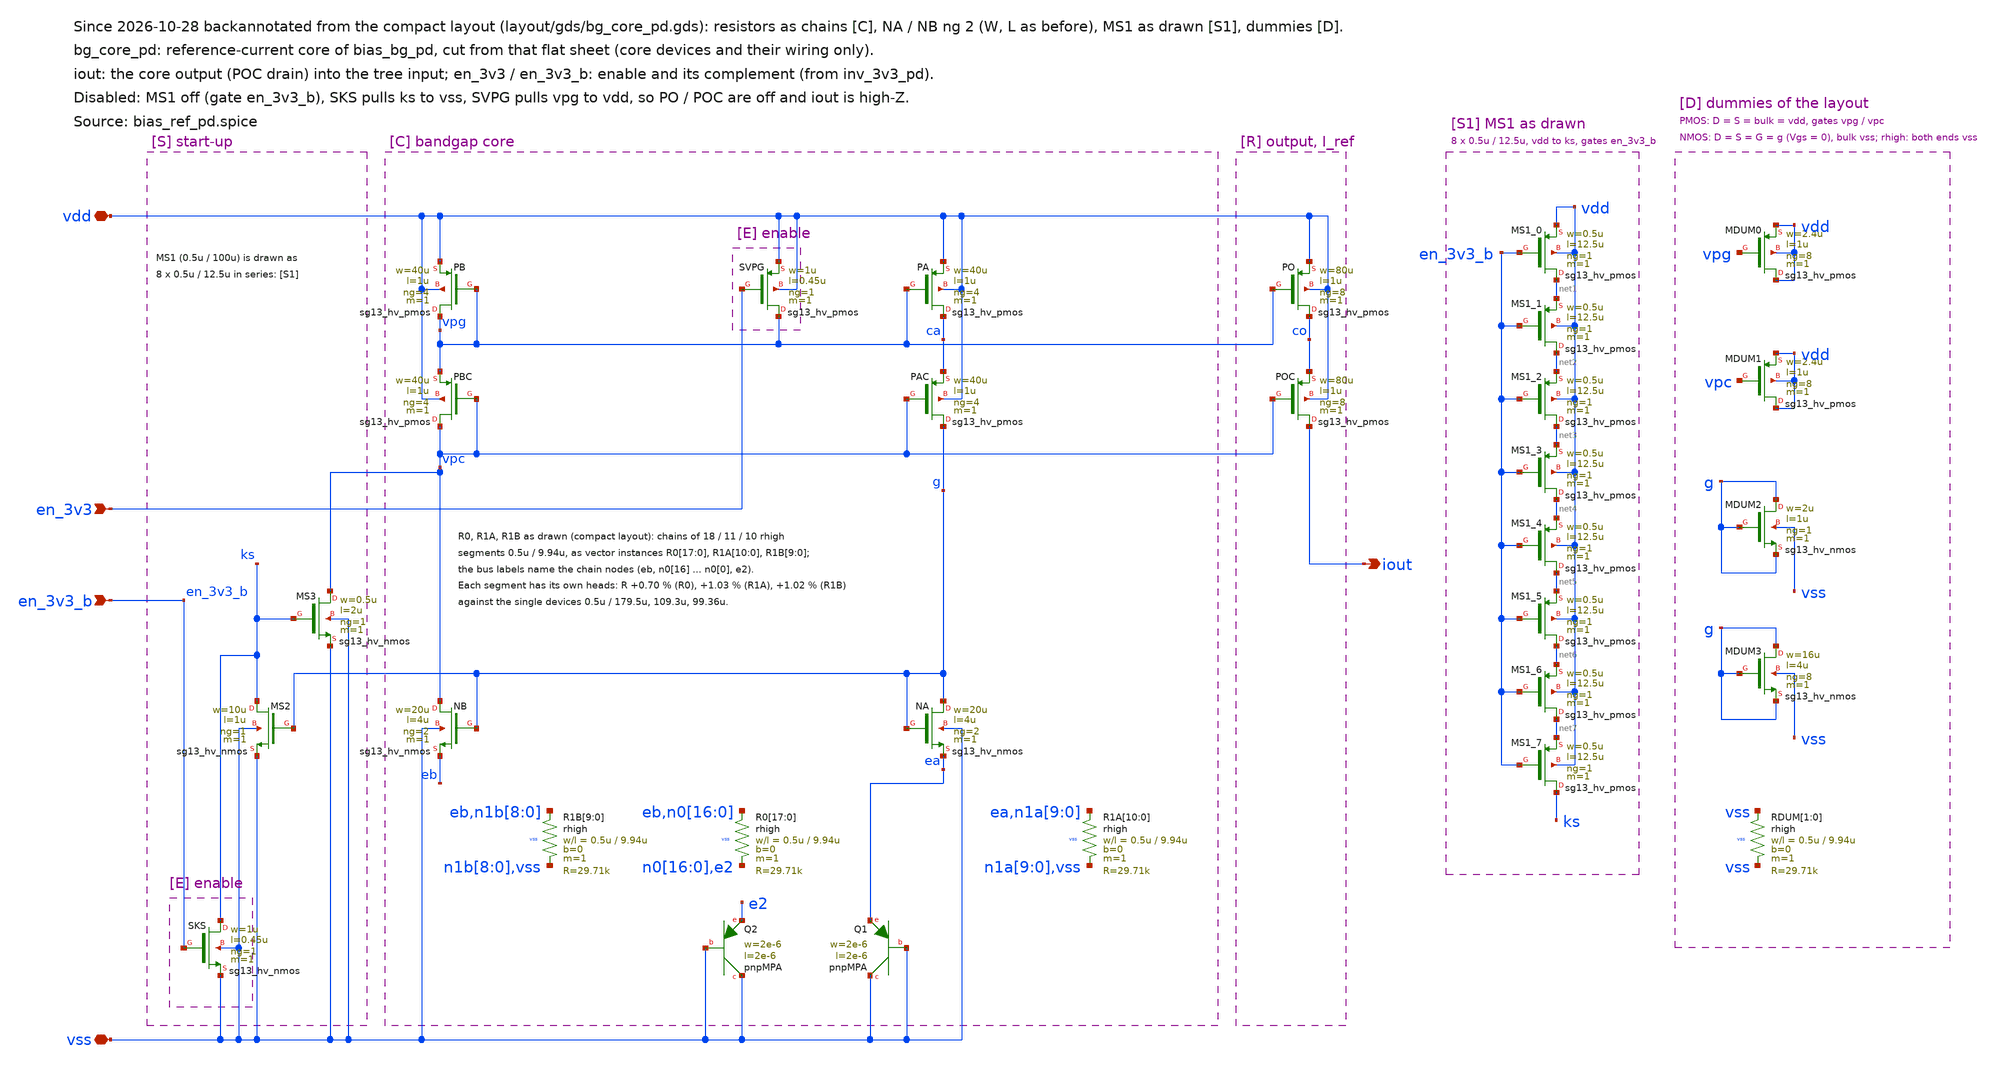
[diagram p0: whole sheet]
** sch_path: macros/bg_core_pd/schematic/xschem/bg_core_pd.sch
**.subckt bg_core_pd vdd vss en_3v3 en_3v3_b iout
*.iopin vdd
*.iopin vss
*.ipin en_3v3
*.ipin en_3v3_b
*.opin iout
XMS2 ks g vss vss sg13_hv_nmos w=10u l=1u ng=1 m=1 mm_ok=1
XMS3 vpc ks vss vss sg13_hv_nmos w=0.5u l=2u ng=1 m=1 mm_ok=1
XPB vpg vpg vdd vdd sg13_hv_pmos w=40u l=1u ng=4 m=1 mm_ok=1
XPBC vpc vpc vpg vdd sg13_hv_pmos w=40u l=1u ng=4 m=1 mm_ok=1
XNB vpc g eb vss sg13_hv_nmos w=20u l=4u ng=2 m=1 mm_ok=1
XQ2 vss vss e2 pnpMPA a=4p p=8u m=8
XPA ca vpg vdd vdd sg13_hv_pmos w=40u l=1u ng=4 m=1 mm_ok=1
XPAC g vpc ca vdd sg13_hv_pmos w=40u l=1u ng=4 m=1 mm_ok=1
XNA g g ea vss sg13_hv_nmos w=20u l=4u ng=2 m=1 mm_ok=1
XQ1 vss vss ea pnpMPA a=4p p=8u m=1
XPO co vpg vdd vdd sg13_hv_pmos w=80u l=1u ng=8 m=1 mm_ok=1
XPOC iout vpc co vdd sg13_hv_pmos w=80u l=1u ng=8 m=1 mm_ok=1
XSKS ks en_3v3_b vss vss sg13_hv_nmos w=1u l=0.45u ng=1 m=1 mm_ok=1
XSVPG vpg en_3v3 vdd vdd sg13_hv_pmos w=1u l=0.45u ng=1 m=1 mm_ok=1
XR1B[9] eb n1b[8] vss rhigh w=0.5u l=9.94u m=1 b=0 mm_ok=1
XR1B[8] n1b[8] n1b[7] vss rhigh w=0.5u l=9.94u m=1 b=0 mm_ok=1
XR1B[7] n1b[7] n1b[6] vss rhigh w=0.5u l=9.94u m=1 b=0 mm_ok=1
XR1B[6] n1b[6] n1b[5] vss rhigh w=0.5u l=9.94u m=1 b=0 mm_ok=1
XR1B[5] n1b[5] n1b[4] vss rhigh w=0.5u l=9.94u m=1 b=0 mm_ok=1
XR1B[4] n1b[4] n1b[3] vss rhigh w=0.5u l=9.94u m=1 b=0 mm_ok=1
XR1B[3] n1b[3] n1b[2] vss rhigh w=0.5u l=9.94u m=1 b=0 mm_ok=1
XR1B[2] n1b[2] n1b[1] vss rhigh w=0.5u l=9.94u m=1 b=0 mm_ok=1
XR1B[1] n1b[1] n1b[0] vss rhigh w=0.5u l=9.94u m=1 b=0 mm_ok=1
XR1B[0] n1b[0] vss vss rhigh w=0.5u l=9.94u m=1 b=0 mm_ok=1
XR0[17] eb n0[16] vss rhigh w=0.5u l=9.94u m=1 b=0 mm_ok=1
XR0[16] n0[16] n0[15] vss rhigh w=0.5u l=9.94u m=1 b=0 mm_ok=1
XR0[15] n0[15] n0[14] vss rhigh w=0.5u l=9.94u m=1 b=0 mm_ok=1
XR0[14] n0[14] n0[13] vss rhigh w=0.5u l=9.94u m=1 b=0 mm_ok=1
XR0[13] n0[13] n0[12] vss rhigh w=0.5u l=9.94u m=1 b=0 mm_ok=1
XR0[12] n0[12] n0[11] vss rhigh w=0.5u l=9.94u m=1 b=0 mm_ok=1
XR0[11] n0[11] n0[10] vss rhigh w=0.5u l=9.94u m=1 b=0 mm_ok=1
XR0[10] n0[10] n0[9] vss rhigh w=0.5u l=9.94u m=1 b=0 mm_ok=1
XR0[9] n0[9] n0[8] vss rhigh w=0.5u l=9.94u m=1 b=0 mm_ok=1
XR0[8] n0[8] n0[7] vss rhigh w=0.5u l=9.94u m=1 b=0 mm_ok=1
XR0[7] n0[7] n0[6] vss rhigh w=0.5u l=9.94u m=1 b=0 mm_ok=1
XR0[6] n0[6] n0[5] vss rhigh w=0.5u l=9.94u m=1 b=0 mm_ok=1
XR0[5] n0[5] n0[4] vss rhigh w=0.5u l=9.94u m=1 b=0 mm_ok=1
XR0[4] n0[4] n0[3] vss rhigh w=0.5u l=9.94u m=1 b=0 mm_ok=1
XR0[3] n0[3] n0[2] vss rhigh w=0.5u l=9.94u m=1 b=0 mm_ok=1
XR0[2] n0[2] n0[1] vss rhigh w=0.5u l=9.94u m=1 b=0 mm_ok=1
XR0[1] n0[1] n0[0] vss rhigh w=0.5u l=9.94u m=1 b=0 mm_ok=1
XR0[0] n0[0] e2 vss rhigh w=0.5u l=9.94u m=1 b=0 mm_ok=1
XR1A[10] ea n1a[9] vss rhigh w=0.5u l=9.94u m=1 b=0 mm_ok=1
XR1A[9] n1a[9] n1a[8] vss rhigh w=0.5u l=9.94u m=1 b=0 mm_ok=1
XR1A[8] n1a[8] n1a[7] vss rhigh w=0.5u l=9.94u m=1 b=0 mm_ok=1
XR1A[7] n1a[7] n1a[6] vss rhigh w=0.5u l=9.94u m=1 b=0 mm_ok=1
XR1A[6] n1a[6] n1a[5] vss rhigh w=0.5u l=9.94u m=1 b=0 mm_ok=1
XR1A[5] n1a[5] n1a[4] vss rhigh w=0.5u l=9.94u m=1 b=0 mm_ok=1
XR1A[4] n1a[4] n1a[3] vss rhigh w=0.5u l=9.94u m=1 b=0 mm_ok=1
XR1A[3] n1a[3] n1a[2] vss rhigh w=0.5u l=9.94u m=1 b=0 mm_ok=1
XR1A[2] n1a[2] n1a[1] vss rhigh w=0.5u l=9.94u m=1 b=0 mm_ok=1
XR1A[1] n1a[1] n1a[0] vss rhigh w=0.5u l=9.94u m=1 b=0 mm_ok=1
XR1A[0] n1a[0] vss vss rhigh w=0.5u l=9.94u m=1 b=0 mm_ok=1
XMS1_0 net1 en_3v3_b vdd vdd sg13_hv_pmos w=0.5u l=12.5u ng=1 m=1 mm_ok=1
XMS1_1 net2 en_3v3_b net1 vdd sg13_hv_pmos w=0.5u l=12.5u ng=1 m=1 mm_ok=1
XMS1_2 net3 en_3v3_b net2 vdd sg13_hv_pmos w=0.5u l=12.5u ng=1 m=1 mm_ok=1
XMS1_3 net4 en_3v3_b net3 vdd sg13_hv_pmos w=0.5u l=12.5u ng=1 m=1 mm_ok=1
XMS1_4 net5 en_3v3_b net4 vdd sg13_hv_pmos w=0.5u l=12.5u ng=1 m=1 mm_ok=1
XMS1_5 net6 en_3v3_b net5 vdd sg13_hv_pmos w=0.5u l=12.5u ng=1 m=1 mm_ok=1
XMS1_6 net7 en_3v3_b net6 vdd sg13_hv_pmos w=0.5u l=12.5u ng=1 m=1 mm_ok=1
XMS1_7 ks en_3v3_b net7 vdd sg13_hv_pmos w=0.5u l=12.5u ng=1 m=1 mm_ok=1
XMDUM0 vdd vpg vdd vdd sg13_hv_pmos w=2.4u l=1u ng=8 m=1 mm_ok=1
XMDUM1 vdd vpc vdd vdd sg13_hv_pmos w=2.4u l=1u ng=8 m=1 mm_ok=1
XMDUM2 g g g vss sg13_hv_nmos w=2u l=1u ng=1 m=1 mm_ok=1
XMDUM3 g g g vss sg13_hv_nmos w=16u l=4u ng=8 m=1 mm_ok=1
XRDUM[1] vss vss vss rhigh w=0.5u l=9.94u m=1 b=0 mm_ok=1
XRDUM[0] vss vss vss rhigh w=0.5u l=9.94u m=1 b=0 mm_ok=1
**.ends
.end
